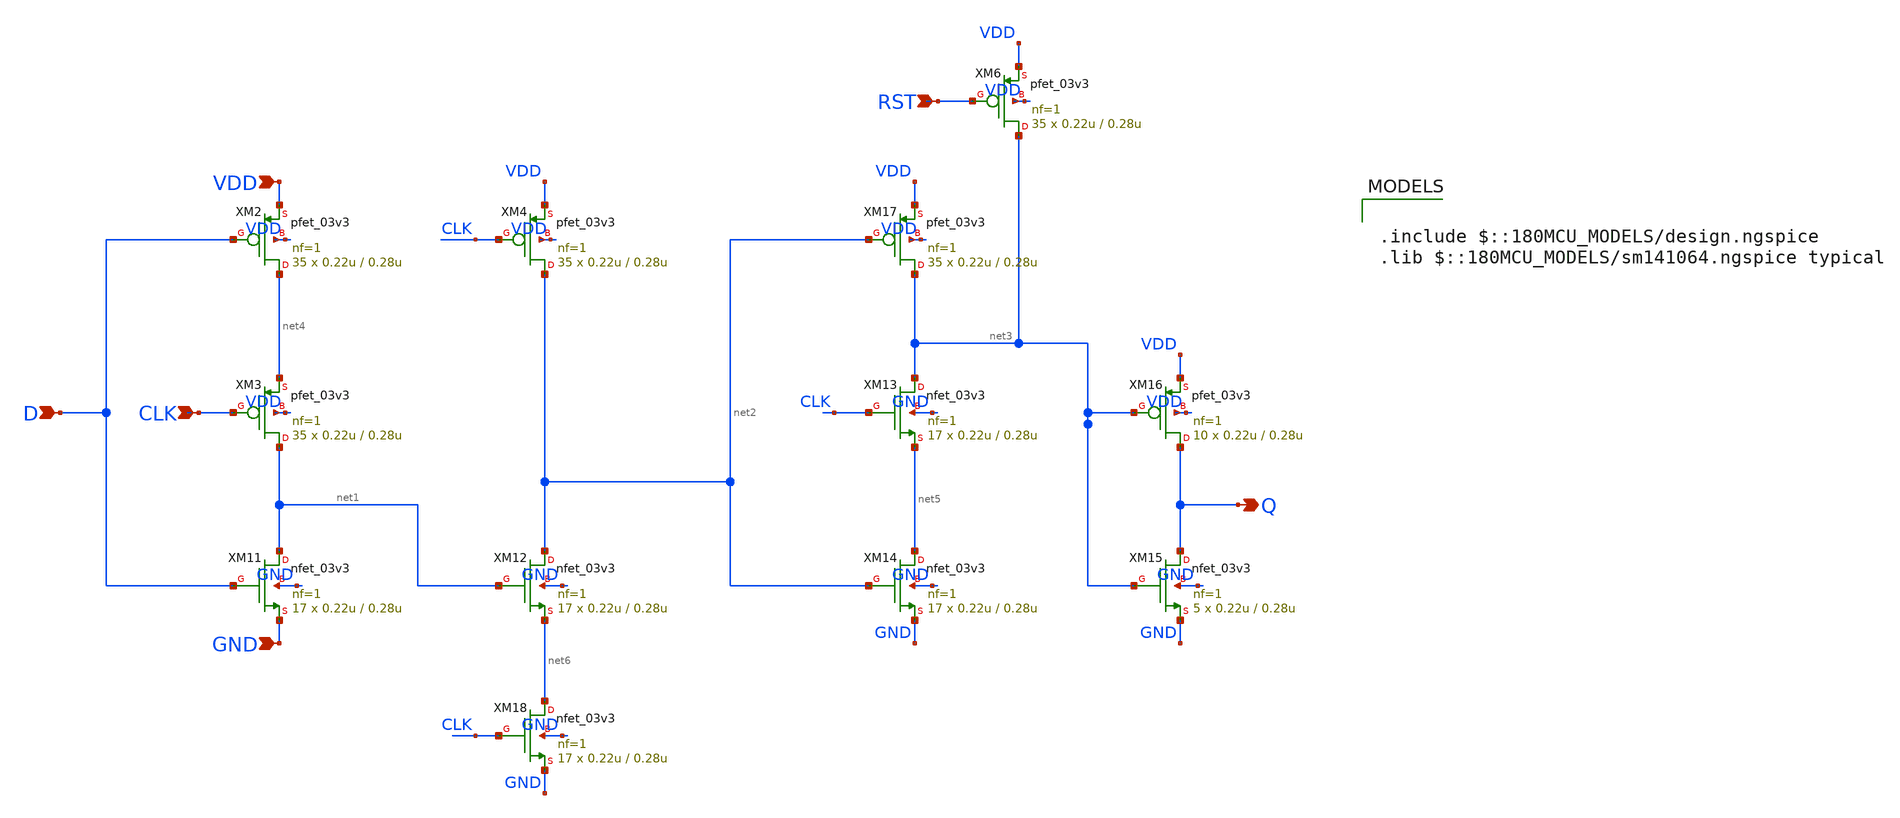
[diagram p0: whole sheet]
** sch_path: blocks/adc/encoder/tb/fast_dff_tb.sch
**.subckt fast_dff_tb Q D CLK RST VDD GND
*.opin Q
*.ipin D
*.ipin CLK
*.ipin RST
*.ipin VDD
*.ipin GND
XM2 net4 D VDD VDD pfet_03v3 L=0.28u W=0.22u nf=1 ad='int((nf+1)/2) * W/nf * 0.18u' as='int((nf+2)/2) * W/nf * 0.18u'
+ pd='2*int((nf+1)/2) * (W/nf + 0.18u)' ps='2*int((nf+2)/2) * (W/nf + 0.18u)' nrd='0.18u / W' nrs='0.18u / W'
+ sa=0 sb=0 sd=0 m=35
XM3 net1 CLK net4 VDD pfet_03v3 L=0.28u W=0.22u nf=1 ad='int((nf+1)/2) * W/nf * 0.18u' as='int((nf+2)/2) * W/nf * 0.18u'
+ pd='2*int((nf+1)/2) * (W/nf + 0.18u)' ps='2*int((nf+2)/2) * (W/nf + 0.18u)' nrd='0.18u / W' nrs='0.18u / W'
+ sa=0 sb=0 sd=0 m=35
XM4 net2 CLK VDD VDD pfet_03v3 L=0.28u W=0.22u nf=1 ad='int((nf+1)/2) * W/nf * 0.18u' as='int((nf+2)/2) * W/nf * 0.18u'
+ pd='2*int((nf+1)/2) * (W/nf + 0.18u)' ps='2*int((nf+2)/2) * (W/nf + 0.18u)' nrd='0.18u / W' nrs='0.18u / W'
+ sa=0 sb=0 sd=0 m=35
XM6 net3 RST VDD VDD pfet_03v3 L=0.28u W=0.22u nf=1 ad='int((nf+1)/2) * W/nf * 0.18u' as='int((nf+2)/2) * W/nf * 0.18u'
+ pd='2*int((nf+1)/2) * (W/nf + 0.18u)' ps='2*int((nf+2)/2) * (W/nf + 0.18u)' nrd='0.18u / W' nrs='0.18u / W'
+ sa=0 sb=0 sd=0 m=35
XM11 net1 D GND GND nfet_03v3 L=0.28u W=0.22u nf=1 ad='int((nf+1)/2) * W/nf * 0.18u' as='int((nf+2)/2) * W/nf * 0.18u'
+ pd='2*int((nf+1)/2) * (W/nf + 0.18u)' ps='2*int((nf+2)/2) * (W/nf + 0.18u)' nrd='0.18u / W' nrs='0.18u / W'
+ sa=0 sb=0 sd=0 m=17
XM12 net2 net1 net6 GND nfet_03v3 L=0.28u W=0.22u nf=1 ad='int((nf+1)/2) * W/nf * 0.18u' as='int((nf+2)/2) * W/nf * 0.18u'
+ pd='2*int((nf+1)/2) * (W/nf + 0.18u)' ps='2*int((nf+2)/2) * (W/nf + 0.18u)' nrd='0.18u / W' nrs='0.18u / W'
+ sa=0 sb=0 sd=0 m=17
XM13 net3 CLK net5 GND nfet_03v3 L=0.28u W=0.22u nf=1 ad='int((nf+1)/2) * W/nf * 0.18u' as='int((nf+2)/2) * W/nf * 0.18u'
+ pd='2*int((nf+1)/2) * (W/nf + 0.18u)' ps='2*int((nf+2)/2) * (W/nf + 0.18u)' nrd='0.18u / W' nrs='0.18u / W'
+ sa=0 sb=0 sd=0 m=17
XM14 net5 net2 GND GND nfet_03v3 L=0.28u W=0.22u nf=1 ad='int((nf+1)/2) * W/nf * 0.18u' as='int((nf+2)/2) * W/nf * 0.18u'
+ pd='2*int((nf+1)/2) * (W/nf + 0.18u)' ps='2*int((nf+2)/2) * (W/nf + 0.18u)' nrd='0.18u / W' nrs='0.18u / W'
+ sa=0 sb=0 sd=0 m=17
XM15 Q net3 GND GND nfet_03v3 L=0.28u W=0.22u nf=1 ad='int((nf+1)/2) * W/nf * 0.18u' as='int((nf+2)/2) * W/nf * 0.18u'
+ pd='2*int((nf+1)/2) * (W/nf + 0.18u)' ps='2*int((nf+2)/2) * (W/nf + 0.18u)' nrd='0.18u / W' nrs='0.18u / W'
+ sa=0 sb=0 sd=0 m=5
XM16 Q net3 VDD VDD pfet_03v3 L=0.28u W=0.22u nf=1 ad='int((nf+1)/2) * W/nf * 0.18u' as='int((nf+2)/2) * W/nf * 0.18u'
+ pd='2*int((nf+1)/2) * (W/nf + 0.18u)' ps='2*int((nf+2)/2) * (W/nf + 0.18u)' nrd='0.18u / W' nrs='0.18u / W'
+ sa=0 sb=0 sd=0 m=10
XM17 net3 net2 VDD VDD pfet_03v3 L=0.28u W=0.22u nf=1 ad='int((nf+1)/2) * W/nf * 0.18u' as='int((nf+2)/2) * W/nf * 0.18u'
+ pd='2*int((nf+1)/2) * (W/nf + 0.18u)' ps='2*int((nf+2)/2) * (W/nf + 0.18u)' nrd='0.18u / W' nrs='0.18u / W'
+ sa=0 sb=0 sd=0 m=35
XM18 net6 CLK GND GND nfet_03v3 L=0.28u W=0.22u nf=1 ad='int((nf+1)/2) * W/nf * 0.18u' as='int((nf+2)/2) * W/nf * 0.18u'
+ pd='2*int((nf+1)/2) * (W/nf + 0.18u)' ps='2*int((nf+2)/2) * (W/nf + 0.18u)' nrd='0.18u / W' nrs='0.18u / W'
+ sa=0 sb=0 sd=0 m=17
**** begin user architecture code

.include $::180MCU_MODELS/design.ngspice
.lib $::180MCU_MODELS/sm141064.ngspice typical



V_VDD VDD 0 3.3

V_CLK CLK 0 pulse(0 3.3 0s 10p 10p 240p 500p)
V_D D 0 pwl(0 0 250p 0 260p 3.3 1.25n 3.3 1.26n 0 1.75n 0 1.76n 3.3 2.25n 3.3 2.26n 0 3.25n 0 3.26n
+ 3.3 3.75n 3.3 3.76n 0 4.25n 0 4.26n 3.3 6n 3.3)
V_RST RST 0 pulse(3.3 3.3 0s 10p 10p 240p 500p)
.control
  save CLK D RST Q
  run
  write tspc_dff_rst_test.raw
.endc
.tran 1p 5n



**** end user architecture code
**.ends
.end
